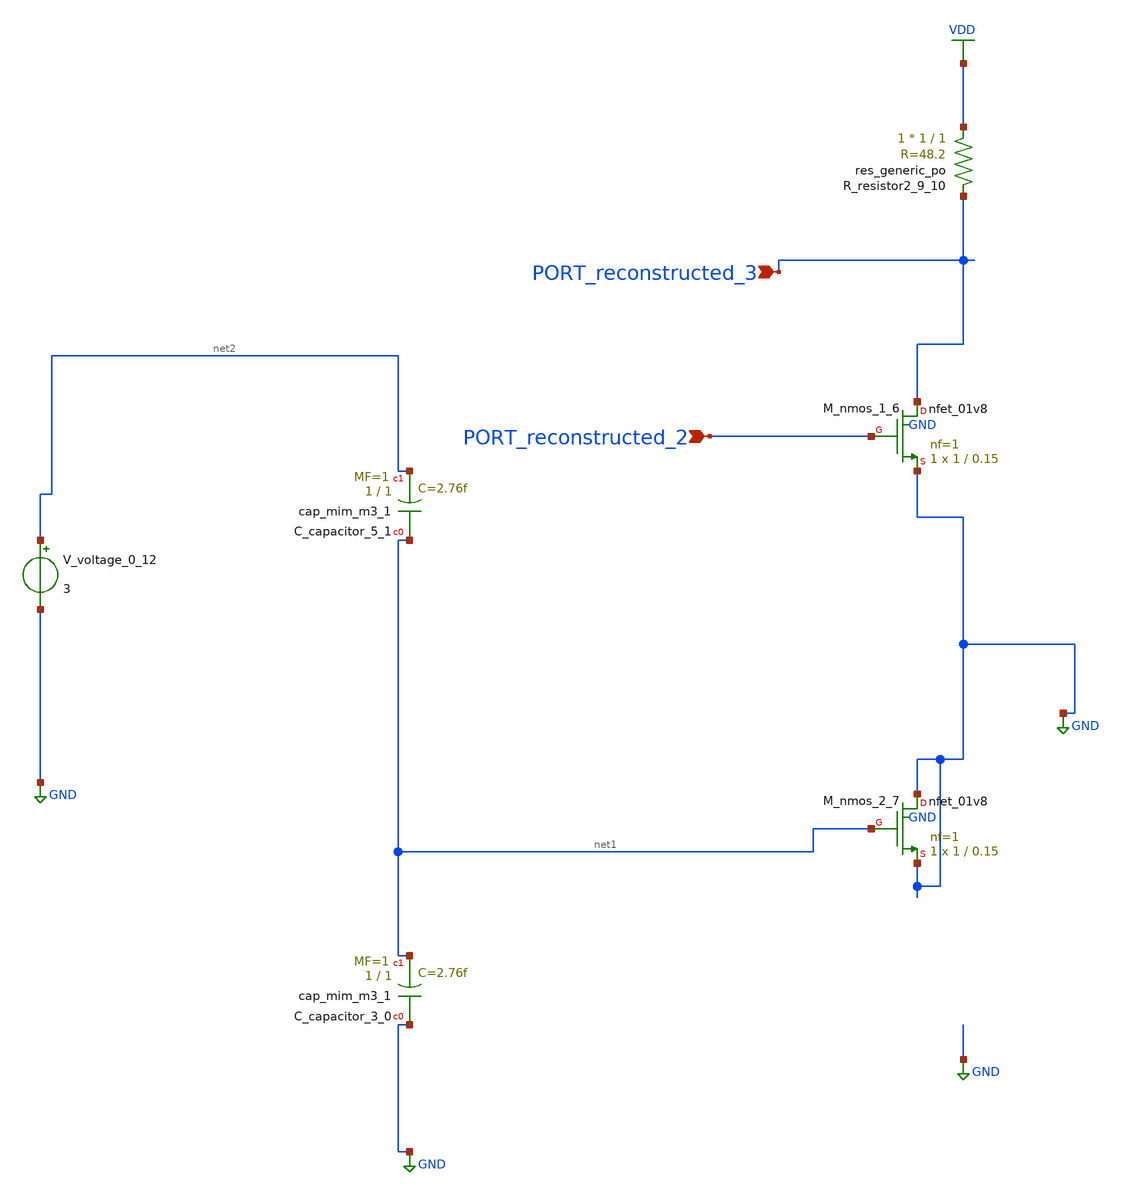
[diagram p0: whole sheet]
** sch_path: schematics/AMSNet/561.sch
**.subckt 561 PORT_reconstructed_2 PORT_reconstructed_3
*.ipin PORT_reconstructed_2
*.ipin PORT_reconstructed_3
XC_capacitor_3_0 GND net1 sky130_fd_pr__cap_mim_m3_1 W=1 L=1 MF=1 m=1
XC_capacitor_5_1 net1 net2 sky130_fd_pr__cap_mim_m3_1 W=1 L=1 MF=1 m=1
XM_nmos_1_6 PORT_reconstructed_3 PORT_reconstructed_2 GND GND sky130_fd_pr__nfet_01v8 L=0.15 W=1 nf=1
+ ad='int((1 + 1)/2) * 1 / 1 * 0.29' as='int((1 + 2)/2) * 1 / 1 * 0.29' pd='2*int((1 + 1)/2) * (1 / 1 + 0.29)'
+ ps='2*int((1 + 2)/2) * (1 / 1 + 0.29)' nrd='0.29 / 1 ' nrs='0.29 / 1 ' sa=0 sb=0 sd=0 mult=1 m=1
XM_nmos_2_7 GND net1 GND GND sky130_fd_pr__nfet_01v8 L=0.15 W=1 nf=1 ad='int((1 + 1)/2) * 1 / 1 * 0.29'
+ as='int((1 + 2)/2) * 1 / 1 * 0.29' pd='2*int((1 + 1)/2) * (1 / 1 + 0.29)' ps='2*int((1 + 2)/2) * (1 / 1 + 0.29)'
+ nrd='0.29 / 1 ' nrs='0.29 / 1 ' sa=0 sb=0 sd=0 mult=1 m=1
XR_resistor2_9_10 VDD PORT_reconstructed_3 sky130_fd_pr__res_generic_po W=1 L=1 m=1
V_voltage_0_12 net2 GND 3
**.ends
.GLOBAL GND
.GLOBAL VDD
.end
